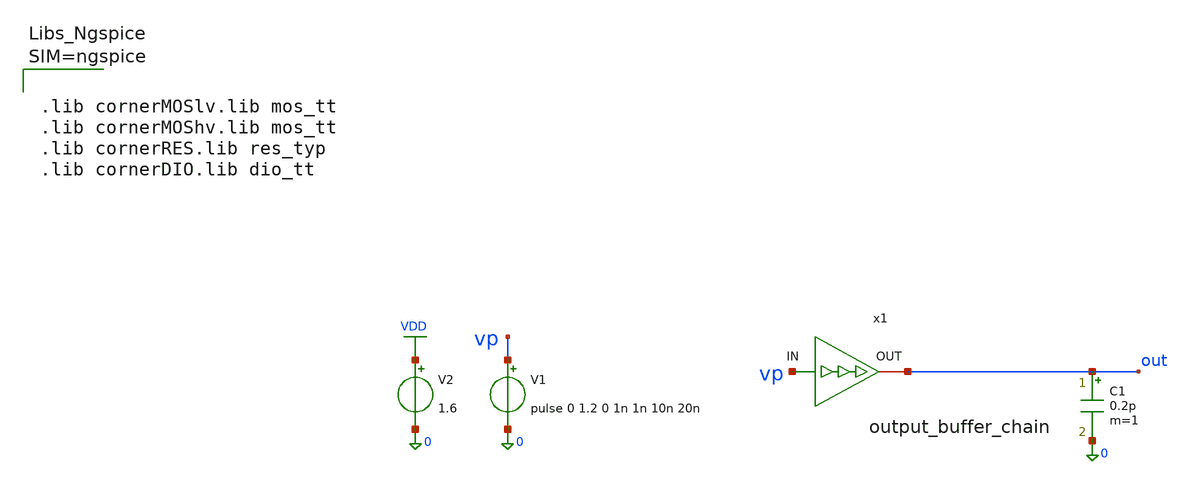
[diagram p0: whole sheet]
** sch_path: analog/output_buffer_chain/testbenches/output_buffer_chain-tb.sch
**.subckt output_buffer_chain-tb
x1 vp out output_buffer_chain
V1 vp 0 pulse 0 1.2 0 1n 1n 10n 20n
V2 VDD 0 1.6
C1 out 0 0.2p m=1
**** begin user architecture code



.lib cornerMOSlv.lib mos_tt
.lib cornerMOShv.lib mos_tt
.lib cornerRES.lib res_typ
.lib cornerDIO.lib dio_tt





.param temp=27
.control
tran 0.2n 100n
* Propagation delay
* input threshold = 0.6 V  (50% of 1.2 V input swing)
* output threshold = 0.8 V (50% of 1.6 V supply)
meas tran tplh trig v(vp)      val=0.6 td=20n rise=1                 targ v(out) val=0.8 td=20n
+ rise=1

meas tran tphl trig v(vp)      val=0.6 td=20n fall=1                 targ v(out) val=0.8 td=20n
+ fall=1

* Output rise / fall time (10%..90% of 1.6 V)
meas tran trise_out trig v(out) val=0.16 td=20n rise=1                      targ v(out) val=1.44
+ td=20n rise=1

meas tran tfall_out trig v(out) val=1.44 td=20n fall=1                      targ v(out) val=0.16
+ td=20n fall=1

write output_buffer_chain-tb.raw vp out
.endc




.param temp=27
.control
ac dec 1000 10meg 100meg
*plot db(v(out)) phase(v(out))
write output_buffer_chain-tb_ac.raw out
.endc


**** end user architecture code
**.ends

* expanding   symbol:  analog/output_buffer_chain/output_buffer_chain.sym # of pins=2
** sym_path: analog/output_buffer_chain/output_buffer_chain.sym
** sch_path: analog/output_buffer_chain/output_buffer_chain.sch
.subckt output_buffer_chain IN OUT
*.ipin IN
*.opin OUT
XM1 net1 IN 0 0 sg13_lv_nmos w=2.0u l=0.45u ng=1 m=1 mm_ok=1
XM2 VDD IN net1 VDD sg13_lv_pmos w=1.0u l=0.45u ng=1 m=1 mm_ok=1
XM3 net2 net1 0 0 sg13_lv_nmos w=4.0u l=0.45u ng=1 m=1 mm_ok=1
XM4 VDD net1 net2 VDD sg13_lv_pmos w=2.0u l=0.45u ng=1 m=1 mm_ok=1
XM5 OUT net2 0 0 sg13_lv_nmos w=16.0u l=0.45u ng=2 m=1 mm_ok=1
XM6 VDD net2 OUT VDD sg13_lv_pmos w=8.0u l=0.45u ng=1 m=1 mm_ok=1
.ends

.GLOBAL VDD
.end
